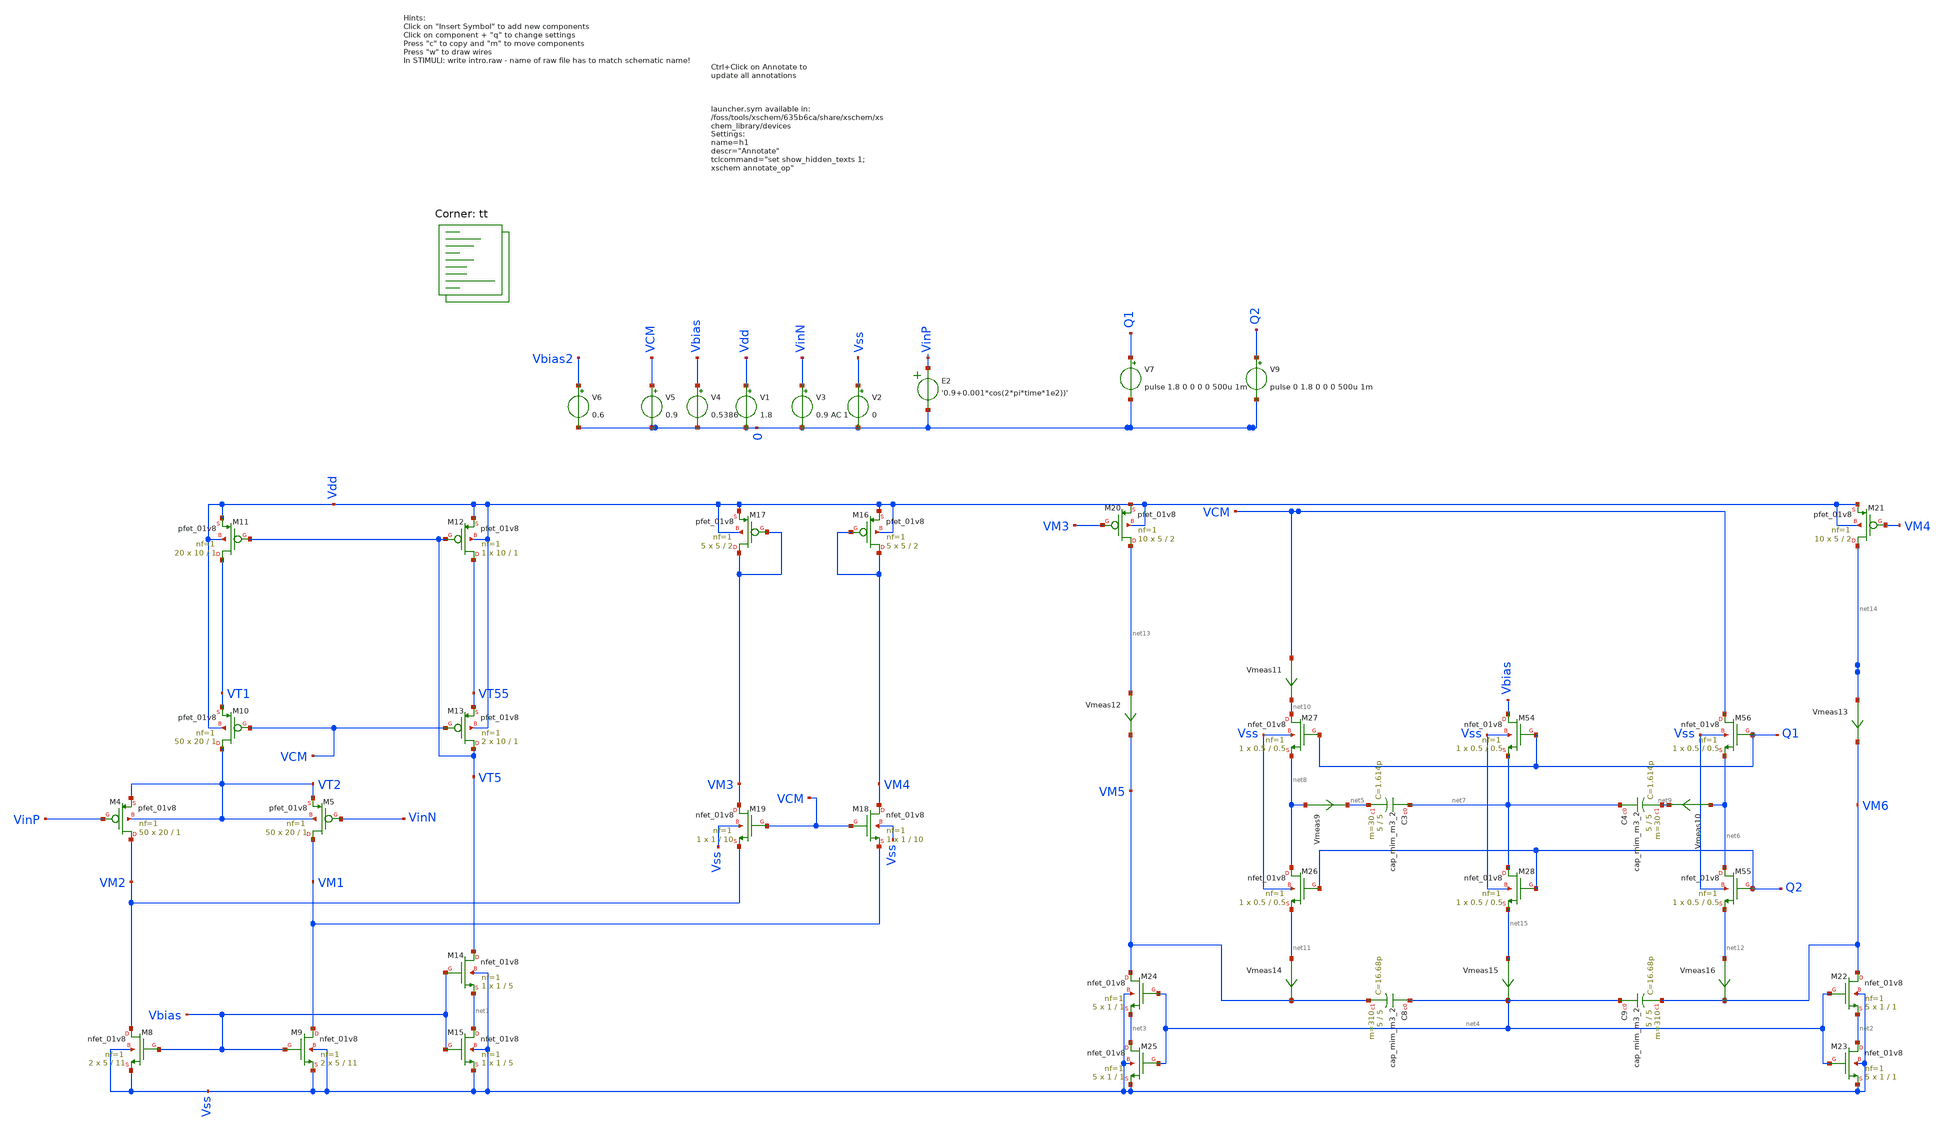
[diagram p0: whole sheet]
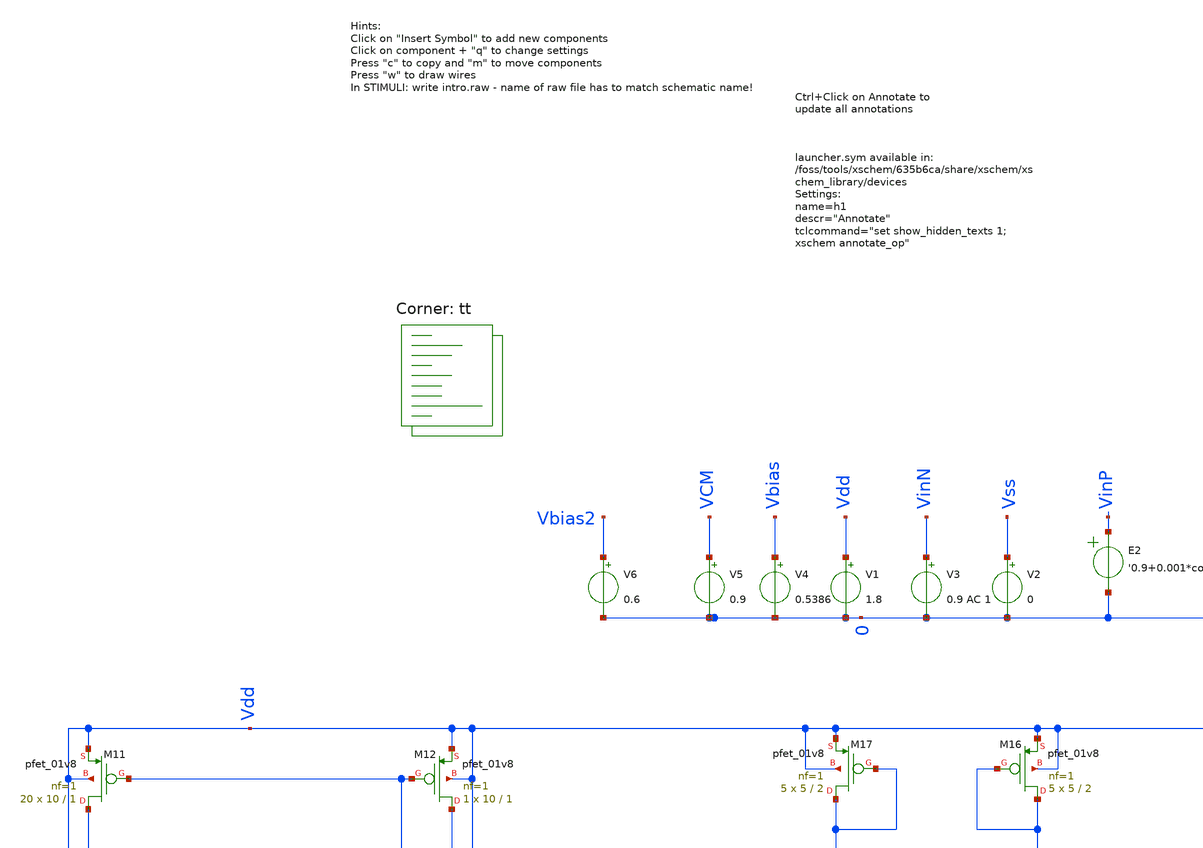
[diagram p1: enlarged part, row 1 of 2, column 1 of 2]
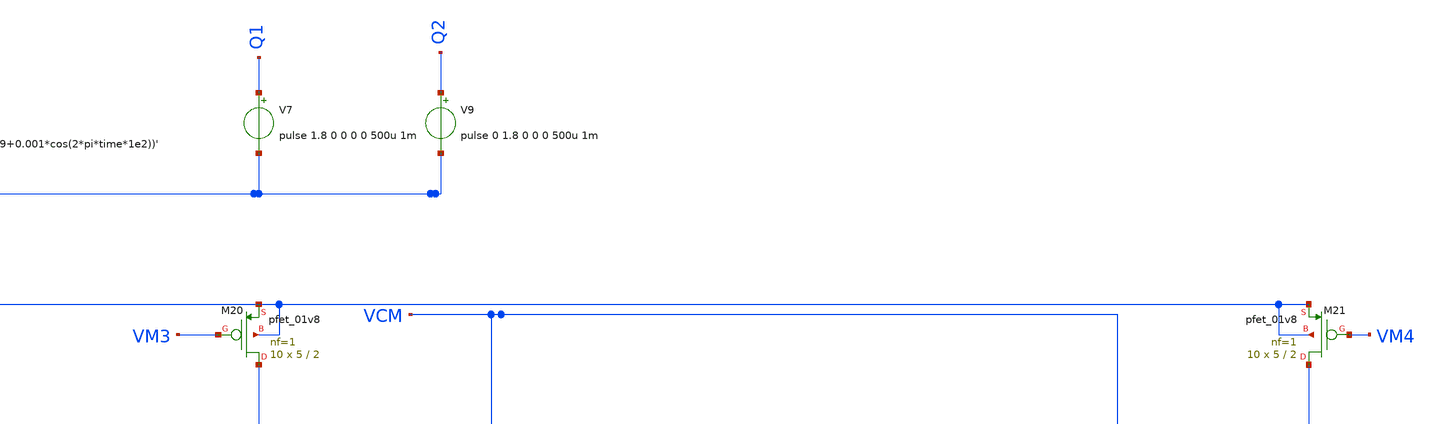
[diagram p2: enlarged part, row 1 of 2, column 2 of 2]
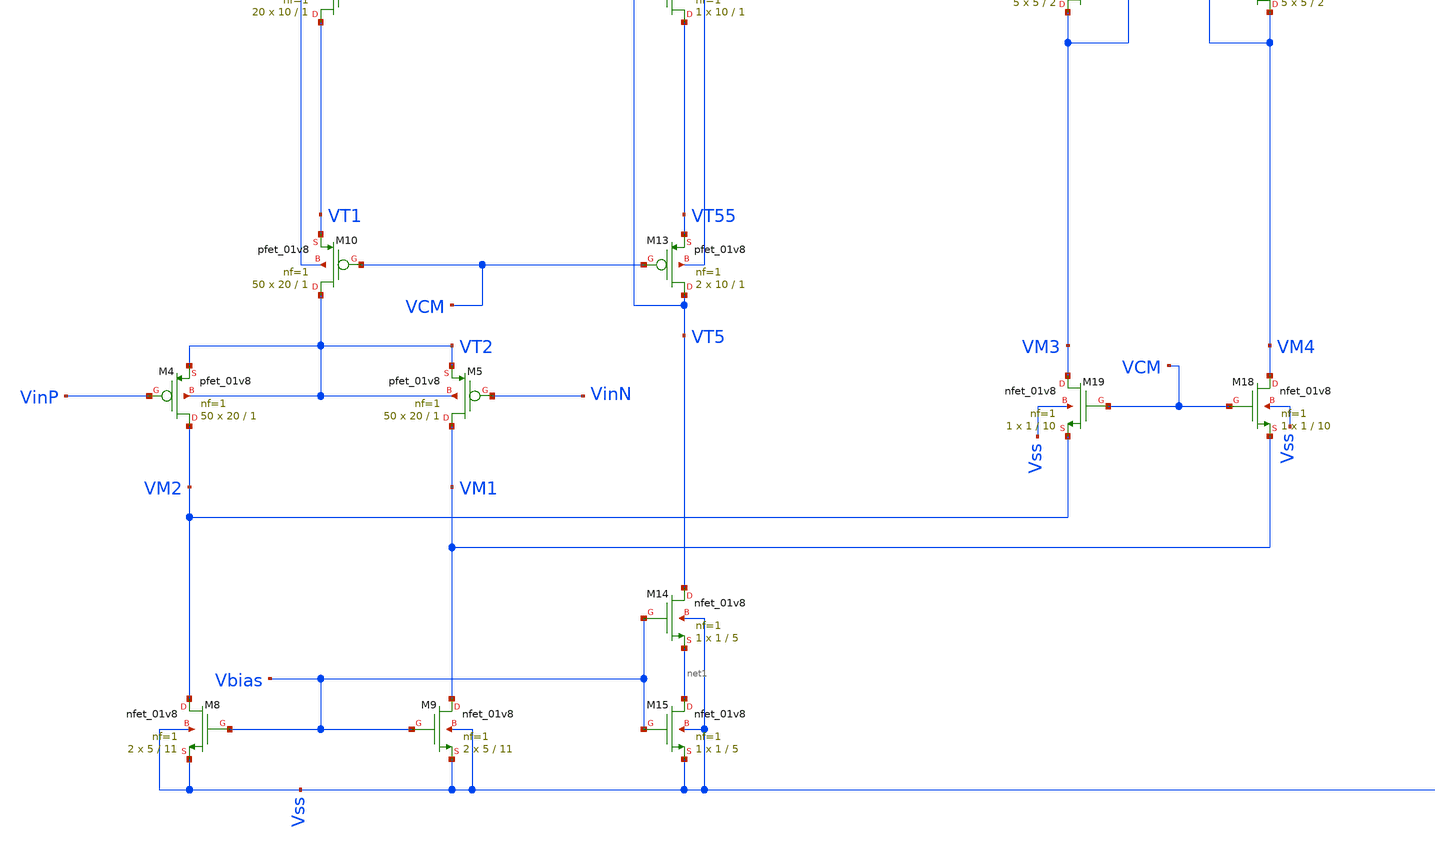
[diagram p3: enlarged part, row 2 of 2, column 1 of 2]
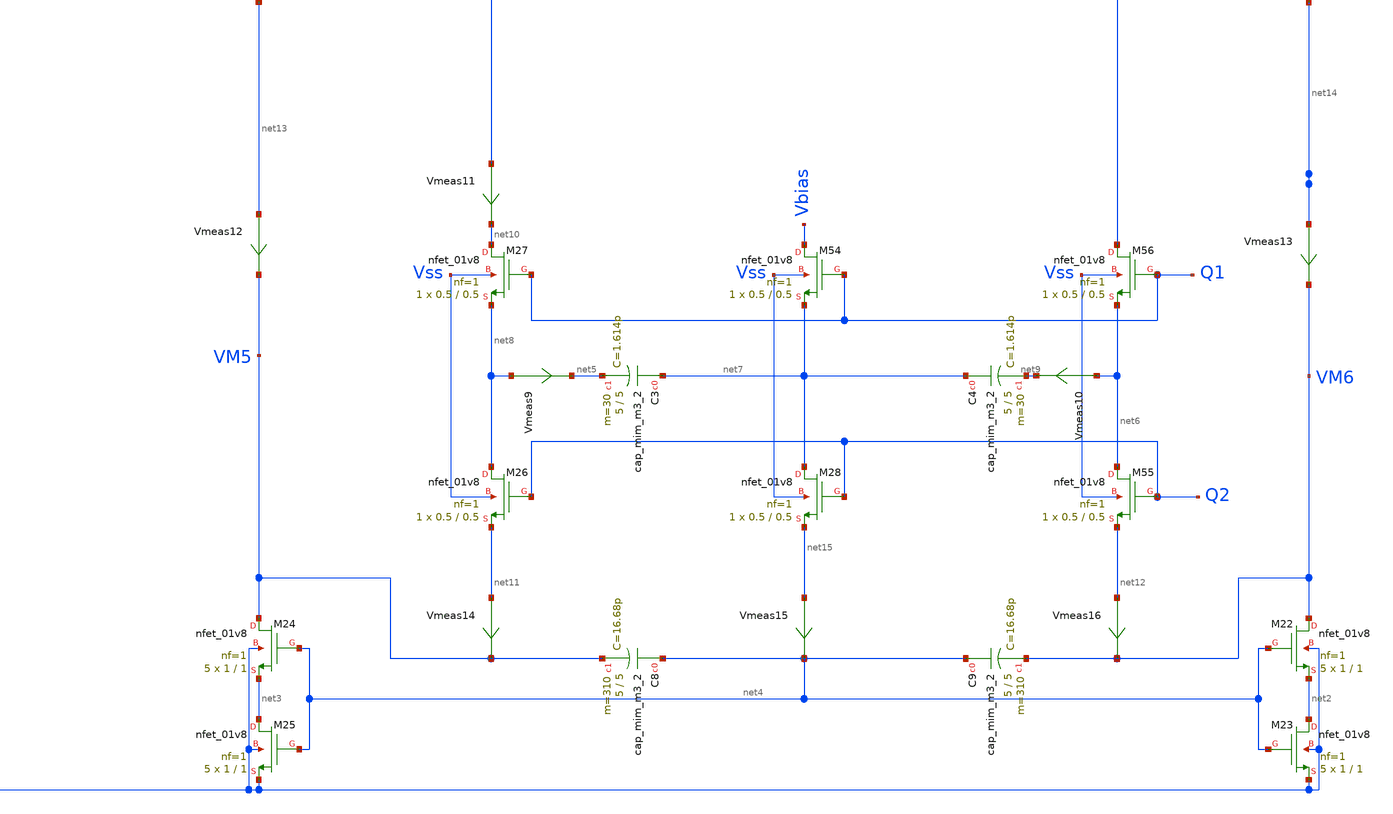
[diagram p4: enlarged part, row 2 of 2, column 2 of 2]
** sch_path: intro.sch
**.subckt intro
XM4 VM2 VinP VT2 VT2 sky130_fd_pr__pfet_01v8 L=1 W=20 nf=1 ad='int((nf+1)/2) * W/nf * 0.29' as='int((nf+2)/2) * W/nf * 0.29'
+ pd='2*int((nf+1)/2) * (W/nf + 0.29)' ps='2*int((nf+2)/2) * (W/nf + 0.29)' nrd='0.29 / W' nrs='0.29 / W'
+ sa=0 sb=0 sd=0 mult=50 m=50
XM5 VM1 VinN VT2 VT2 sky130_fd_pr__pfet_01v8 L=1 W=20 nf=1 ad='int((nf+1)/2) * W/nf * 0.29' as='int((nf+2)/2) * W/nf * 0.29'
+ pd='2*int((nf+1)/2) * (W/nf + 0.29)' ps='2*int((nf+2)/2) * (W/nf + 0.29)' nrd='0.29 / W' nrs='0.29 / W'
+ sa=0 sb=0 sd=0 mult=50 m=50
XM8 VM2 Vbias Vss Vss sky130_fd_pr__nfet_01v8 L=11 W=5 nf=1 ad='int((nf+1)/2) * W/nf * 0.29' as='int((nf+2)/2) * W/nf * 0.29'
+ pd='2*int((nf+1)/2) * (W/nf + 0.29)' ps='2*int((nf+2)/2) * (W/nf + 0.29)' nrd='0.29 / W' nrs='0.29 / W'
+ sa=0 sb=0 sd=0 mult=2 m=2
XM9 VM1 Vbias Vss Vss sky130_fd_pr__nfet_01v8 L=11 W=5 nf=1 ad='int((nf+1)/2) * W/nf * 0.29' as='int((nf+2)/2) * W/nf * 0.29'
+ pd='2*int((nf+1)/2) * (W/nf + 0.29)' ps='2*int((nf+2)/2) * (W/nf + 0.29)' nrd='0.29 / W' nrs='0.29 / W'
+ sa=0 sb=0 sd=0 mult=2 m=2
XM10 VT2 VCM VT1 Vdd sky130_fd_pr__pfet_01v8 L=1 W=20 nf=1 ad='int((nf+1)/2) * W/nf * 0.29' as='int((nf+2)/2) * W/nf * 0.29'
+ pd='2*int((nf+1)/2) * (W/nf + 0.29)' ps='2*int((nf+2)/2) * (W/nf + 0.29)' nrd='0.29 / W' nrs='0.29 / W'
+ sa=0 sb=0 sd=0 mult=50 m=50
XM11 VT1 VT5 Vdd Vdd sky130_fd_pr__pfet_01v8 L=1 W=10 nf=1 ad='int((nf+1)/2) * W/nf * 0.29' as='int((nf+2)/2) * W/nf * 0.29'
+ pd='2*int((nf+1)/2) * (W/nf + 0.29)' ps='2*int((nf+2)/2) * (W/nf + 0.29)' nrd='0.29 / W' nrs='0.29 / W'
+ sa=0 sb=0 sd=0 mult=20 m=20
XM12 VT55 VT5 Vdd Vdd sky130_fd_pr__pfet_01v8 L=1 W=10 nf=1 ad='int((nf+1)/2) * W/nf * 0.29' as='int((nf+2)/2) * W/nf * 0.29'
+ pd='2*int((nf+1)/2) * (W/nf + 0.29)' ps='2*int((nf+2)/2) * (W/nf + 0.29)' nrd='0.29 / W' nrs='0.29 / W'
+ sa=0 sb=0 sd=0 mult=1 m=1
XM13 VT5 VCM VT55 Vdd sky130_fd_pr__pfet_01v8 L=1 W=10 nf=1 ad='int((nf+1)/2) * W/nf * 0.29' as='int((nf+2)/2) * W/nf * 0.29'
+ pd='2*int((nf+1)/2) * (W/nf + 0.29)' ps='2*int((nf+2)/2) * (W/nf + 0.29)' nrd='0.29 / W' nrs='0.29 / W'
+ sa=0 sb=0 sd=0 mult=2 m=2
XM14 VT5 Vbias net1 Vss sky130_fd_pr__nfet_01v8 L=5 W=1 nf=1 ad='int((nf+1)/2) * W/nf * 0.29' as='int((nf+2)/2) * W/nf * 0.29'
+ pd='2*int((nf+1)/2) * (W/nf + 0.29)' ps='2*int((nf+2)/2) * (W/nf + 0.29)' nrd='0.29 / W' nrs='0.29 / W'
+ sa=0 sb=0 sd=0 mult=1 m=1
XM15 net1 Vbias Vss Vss sky130_fd_pr__nfet_01v8 L=5 W=1 nf=1 ad='int((nf+1)/2) * W/nf * 0.29' as='int((nf+2)/2) * W/nf * 0.29'
+ pd='2*int((nf+1)/2) * (W/nf + 0.29)' ps='2*int((nf+2)/2) * (W/nf + 0.29)' nrd='0.29 / W' nrs='0.29 / W'
+ sa=0 sb=0 sd=0 mult=1 m=1
XM16 VM4 VM4 Vdd Vdd sky130_fd_pr__pfet_01v8 L=2 W=5 nf=1 ad='int((nf+1)/2) * W/nf * 0.29' as='int((nf+2)/2) * W/nf * 0.29'
+ pd='2*int((nf+1)/2) * (W/nf + 0.29)' ps='2*int((nf+2)/2) * (W/nf + 0.29)' nrd='0.29 / W' nrs='0.29 / W'
+ sa=0 sb=0 sd=0 mult=5 m=5
XM17 VM3 VM3 Vdd Vdd sky130_fd_pr__pfet_01v8 L=2 W=5 nf=1 ad='int((nf+1)/2) * W/nf * 0.29' as='int((nf+2)/2) * W/nf * 0.29'
+ pd='2*int((nf+1)/2) * (W/nf + 0.29)' ps='2*int((nf+2)/2) * (W/nf + 0.29)' nrd='0.29 / W' nrs='0.29 / W'
+ sa=0 sb=0 sd=0 mult=5 m=5
XM18 VM4 VCM VM1 Vss sky130_fd_pr__nfet_01v8 L=10 W=1 nf=1 ad='int((nf+1)/2) * W/nf * 0.29' as='int((nf+2)/2) * W/nf * 0.29'
+ pd='2*int((nf+1)/2) * (W/nf + 0.29)' ps='2*int((nf+2)/2) * (W/nf + 0.29)' nrd='0.29 / W' nrs='0.29 / W'
+ sa=0 sb=0 sd=0 mult=1 m=1
XM19 VM3 VCM VM2 Vss sky130_fd_pr__nfet_01v8 L=10 W=1 nf=1 ad='int((nf+1)/2) * W/nf * 0.29' as='int((nf+2)/2) * W/nf * 0.29'
+ pd='2*int((nf+1)/2) * (W/nf + 0.29)' ps='2*int((nf+2)/2) * (W/nf + 0.29)' nrd='0.29 / W' nrs='0.29 / W'
+ sa=0 sb=0 sd=0 mult=1 m=1
XM20 net13 VM3 Vdd Vdd sky130_fd_pr__pfet_01v8 L=2 W=5 nf=1 ad='int((nf+1)/2) * W/nf * 0.29' as='int((nf+2)/2) * W/nf * 0.29'
+ pd='2*int((nf+1)/2) * (W/nf + 0.29)' ps='2*int((nf+2)/2) * (W/nf + 0.29)' nrd='0.29 / W' nrs='0.29 / W'
+ sa=0 sb=0 sd=0 mult=10 m=10
XM21 net14 VM4 Vdd Vdd sky130_fd_pr__pfet_01v8 L=2 W=5 nf=1 ad='int((nf+1)/2) * W/nf * 0.29' as='int((nf+2)/2) * W/nf * 0.29'
+ pd='2*int((nf+1)/2) * (W/nf + 0.29)' ps='2*int((nf+2)/2) * (W/nf + 0.29)' nrd='0.29 / W' nrs='0.29 / W'
+ sa=0 sb=0 sd=0 mult=10 m=10
XM22 VM6 net4 net2 Vss sky130_fd_pr__nfet_01v8 L=1 W=1 nf=1 ad='int((nf+1)/2) * W/nf * 0.29' as='int((nf+2)/2) * W/nf * 0.29'
+ pd='2*int((nf+1)/2) * (W/nf + 0.29)' ps='2*int((nf+2)/2) * (W/nf + 0.29)' nrd='0.29 / W' nrs='0.29 / W'
+ sa=0 sb=0 sd=0 mult=5 m=5
XM23 net2 net4 Vss Vss sky130_fd_pr__nfet_01v8 L=1 W=1 nf=1 ad='int((nf+1)/2) * W/nf * 0.29' as='int((nf+2)/2) * W/nf * 0.29'
+ pd='2*int((nf+1)/2) * (W/nf + 0.29)' ps='2*int((nf+2)/2) * (W/nf + 0.29)' nrd='0.29 / W' nrs='0.29 / W'
+ sa=0 sb=0 sd=0 mult=5 m=5
XM24 VM5 net4 net3 Vss sky130_fd_pr__nfet_01v8 L=1 W=1 nf=1 ad='int((nf+1)/2) * W/nf * 0.29' as='int((nf+2)/2) * W/nf * 0.29'
+ pd='2*int((nf+1)/2) * (W/nf + 0.29)' ps='2*int((nf+2)/2) * (W/nf + 0.29)' nrd='0.29 / W' nrs='0.29 / W'
+ sa=0 sb=0 sd=0 mult=5 m=5
XM25 net3 net4 Vss Vss sky130_fd_pr__nfet_01v8 L=1 W=1 nf=1 ad='int((nf+1)/2) * W/nf * 0.29' as='int((nf+2)/2) * W/nf * 0.29'
+ pd='2*int((nf+1)/2) * (W/nf + 0.29)' ps='2*int((nf+2)/2) * (W/nf + 0.29)' nrd='0.29 / W' nrs='0.29 / W'
+ sa=0 sb=0 sd=0 mult=5 m=5
E2 VinP 0 VOL=' '0.9+0.001*cos(2*pi*time*1e2))' '
V1 Vdd 0 1.8
V2 Vss 0 0
V3 VinN 0 0.9 AC 1
V4 Vbias 0 0.5386
V5 VCM 0 0.9
V6 Vbias2 0 0.6
XC3 net7 net5 sky130_fd_pr__cap_mim_m3_2 W=5 L=5 MF=30 m=30
XC4 net7 net9 sky130_fd_pr__cap_mim_m3_2 W=5 L=5 MF=30 m=30
XC8 net4 VM5 sky130_fd_pr__cap_mim_m3_2 W=5 L=5 MF=310 m=310
XC9 net4 VM6 sky130_fd_pr__cap_mim_m3_2 W=5 L=5 MF=310 m=310
XM26 net8 Q2 net11 Vss sky130_fd_pr__nfet_01v8 L=0.5 W=0.5 nf=1 ad='int((nf+1)/2) * W/nf * 0.29' as='int((nf+2)/2) * W/nf * 0.29'
+ pd='2*int((nf+1)/2) * (W/nf + 0.29)' ps='2*int((nf+2)/2) * (W/nf + 0.29)' nrd='0.29 / W' nrs='0.29 / W'
+ sa=0 sb=0 sd=0 mult=1 m=1
XM27 net10 Q1 net8 Vss sky130_fd_pr__nfet_01v8 L=0.5 W=0.5 nf=1 ad='int((nf+1)/2) * W/nf * 0.29' as='int((nf+2)/2) * W/nf * 0.29'
+ pd='2*int((nf+1)/2) * (W/nf + 0.29)' ps='2*int((nf+2)/2) * (W/nf + 0.29)' nrd='0.29 / W' nrs='0.29 / W'
+ sa=0 sb=0 sd=0 mult=1 m=1
XM28 net7 Q2 net15 Vss sky130_fd_pr__nfet_01v8 L=0.5 W=0.5 nf=1 ad='int((nf+1)/2) * W/nf * 0.29' as='int((nf+2)/2) * W/nf * 0.29'
+ pd='2*int((nf+1)/2) * (W/nf + 0.29)' ps='2*int((nf+2)/2) * (W/nf + 0.29)' nrd='0.29 / W' nrs='0.29 / W'
+ sa=0 sb=0 sd=0 mult=1 m=1
XM54 Vbias Q1 net7 Vss sky130_fd_pr__nfet_01v8 L=0.5 W=0.5 nf=1 ad='int((nf+1)/2) * W/nf * 0.29' as='int((nf+2)/2) * W/nf * 0.29'
+ pd='2*int((nf+1)/2) * (W/nf + 0.29)' ps='2*int((nf+2)/2) * (W/nf + 0.29)' nrd='0.29 / W' nrs='0.29 / W'
+ sa=0 sb=0 sd=0 mult=1 m=1
XM55 net6 Q2 net12 Vss sky130_fd_pr__nfet_01v8 L=0.5 W=0.5 nf=1 ad='int((nf+1)/2) * W/nf * 0.29' as='int((nf+2)/2) * W/nf * 0.29'
+ pd='2*int((nf+1)/2) * (W/nf + 0.29)' ps='2*int((nf+2)/2) * (W/nf + 0.29)' nrd='0.29 / W' nrs='0.29 / W'
+ sa=0 sb=0 sd=0 mult=1 m=1
XM56 VCM Q1 net6 Vss sky130_fd_pr__nfet_01v8 L=0.5 W=0.5 nf=1 ad='int((nf+1)/2) * W/nf * 0.29' as='int((nf+2)/2) * W/nf * 0.29'
+ pd='2*int((nf+1)/2) * (W/nf + 0.29)' ps='2*int((nf+2)/2) * (W/nf + 0.29)' nrd='0.29 / W' nrs='0.29 / W'
+ sa=0 sb=0 sd=0 mult=1 m=1
Vmeas9 net8 net5 0
.save i(vmeas9)
Vmeas10 net6 net9 0
.save i(vmeas10)
Vmeas11 VCM net10 0
.save i(vmeas11)
Vmeas12 net13 VM5 0
.save i(vmeas12)
Vmeas13 net14 VM6 0
.save i(vmeas13)
Vmeas14 net11 VM5 0
.save i(vmeas14)
Vmeas15 net15 net4 0
.save i(vmeas15)
Vmeas16 net12 VM6 0
.save i(vmeas16)
V9 Q2 0 pulse 0 1.8 0 0 0 500u 1m
V7 Q1 0 pulse 1.8 0 0 0 0 500u 1m
**** begin user architecture code


.options savecurrents
.control



save all
save @m.xm8.msky130_fd_pr__nfet_01v8[vgs]
save @m.xm8.msky130_fd_pr__nfet_01v8[vth]
save @m.xm8.msky130_fd_pr__nfet_01v8[vds]

save @m.xm9.msky130_fd_pr__nfet_01v8[vgs]
save @m.xm9.msky130_fd_pr__nfet_01v8[vth]
save @m.xm9.msky130_fd_pr__nfet_01v8[vds]



save @m.xm16.msky130_fd_pr__pfet_01v8[vgs]
save @m.xm16.msky130_fd_pr__pfet_01v8[vth]
save @m.xm16.msky130_fd_pr__pfet_01v8[vds]


save @m.xm17.msky130_fd_pr__pfet_01v8[vgs]
save @m.xm17.msky130_fd_pr__pfet_01v8[vth]
save @m.xm17.msky130_fd_pr__pfet_01v8[vds]


save @m.xm11.msky130_fd_pr__pfet_01v8[vgs]
save @m.xm11.msky130_fd_pr__pfet_01v8[vth]
save @m.xm11.msky130_fd_pr__pfet_01v8[vds]

save @m.xm12.msky130_fd_pr__pfet_01v8[vgs]
save @m.xm12.msky130_fd_pr__pfet_01v8[vth]
save @m.xm12.msky130_fd_pr__pfet_01v8[vds]

save @m.xm10.msky130_fd_pr__pfet_01v8[vgs]
save @m.xm10.msky130_fd_pr__pfet_01v8[vth]
save @m.xm10.msky130_fd_pr__pfet_01v8[vds]

save @m.xm13.msky130_fd_pr__pfet_01v8[vgs]
save @m.xm13.msky130_fd_pr__pfet_01v8[vth]
save @m.xm13.msky130_fd_pr__pfet_01v8[vds]

save @m.xm1.msky130_fd_pr__pfet_01v8[id]
save @m.xm7.msky130_fd_pr__pfet_01v8[id]
save @m.xm1.msky130_fd_pr__pfet_01v8[id]

save @m.xm4.msky130_fd_pr__pfet_01v8[vgs]
save @m.xm4.msky130_fd_pr__pfet_01v8[vth]
save @m.xm4.msky130_fd_pr__pfet_01v8[vds]

save @m.xm3.msky130_fd_pr__pfet_01v8[vgs]
save @m.xm3.msky130_fd_pr__pfet_01v8[vth]
save @m.xm3.msky130_fd_pr__pfet_01v8[vds]

save @m.xm5.msky130_fd_pr__pfet_01v8[vgs]
save @m.xm5.msky130_fd_pr__pfet_01v8[vth]
save @m.xm5.msky130_fd_pr__pfet_01v8[vds]

save @m.xm3.msky130_fd_pr__pfet_01v8[vgs]
save @m.xm3.msky130_fd_pr__pfet_01v8[vth]
save @m.xm3.msky130_fd_pr__pfet_01v8[vds]

save @m.xm7.msky130_fd_pr__nfet_01v8[vth]

save @m.xm1.msky130_fd_pr__pfet_01v8[vgs]

save @m.xm1.msky130_fd_pr__nfet_01v8_lvt[gm]


save @m.xm1.msky130_fd_pr__nfet_01v8_lvt[gds]
save @m.xm2.msky130_fd_pr__pfet_01v8_lvt[gm]

save @m.xm23.msky130_fd_pr__nfet_01v8[cgs]
save @m.xm4.msky130_fd_pr__pfet_01v8[cgs]
save @m.xm2.msky130_fd_pr__pfet_01v8_lvt[cgs]



save @m.xm2.msky130_fd_pr__pfet_01v8_lvt[gds]


op
remzerovec
write intro.raw
*set appendwrite

*dc V1 0 1.8 0.01
*plot @m.xm1.msky130_fd_pr__nfet_01v8_lvt[id] @m.xm2.msky130_fd_pr__pfet_01v8_lvt[id]
*remzerovec
*write intro.raw

.endc
.control
tran 100u 300m
save all
plot v(VM5)
plot v(VM6)-v(VM5)

noise V(VM5,VM6) V3 dec 100 0.1 100
print inoise_total onoise_total
setplot noise1
plot inoise_spectrum


.endc





.lib $::SKYWATER_MODELS/sky130.lib.spice tt
**** end user architecture code
**.ends
.end
